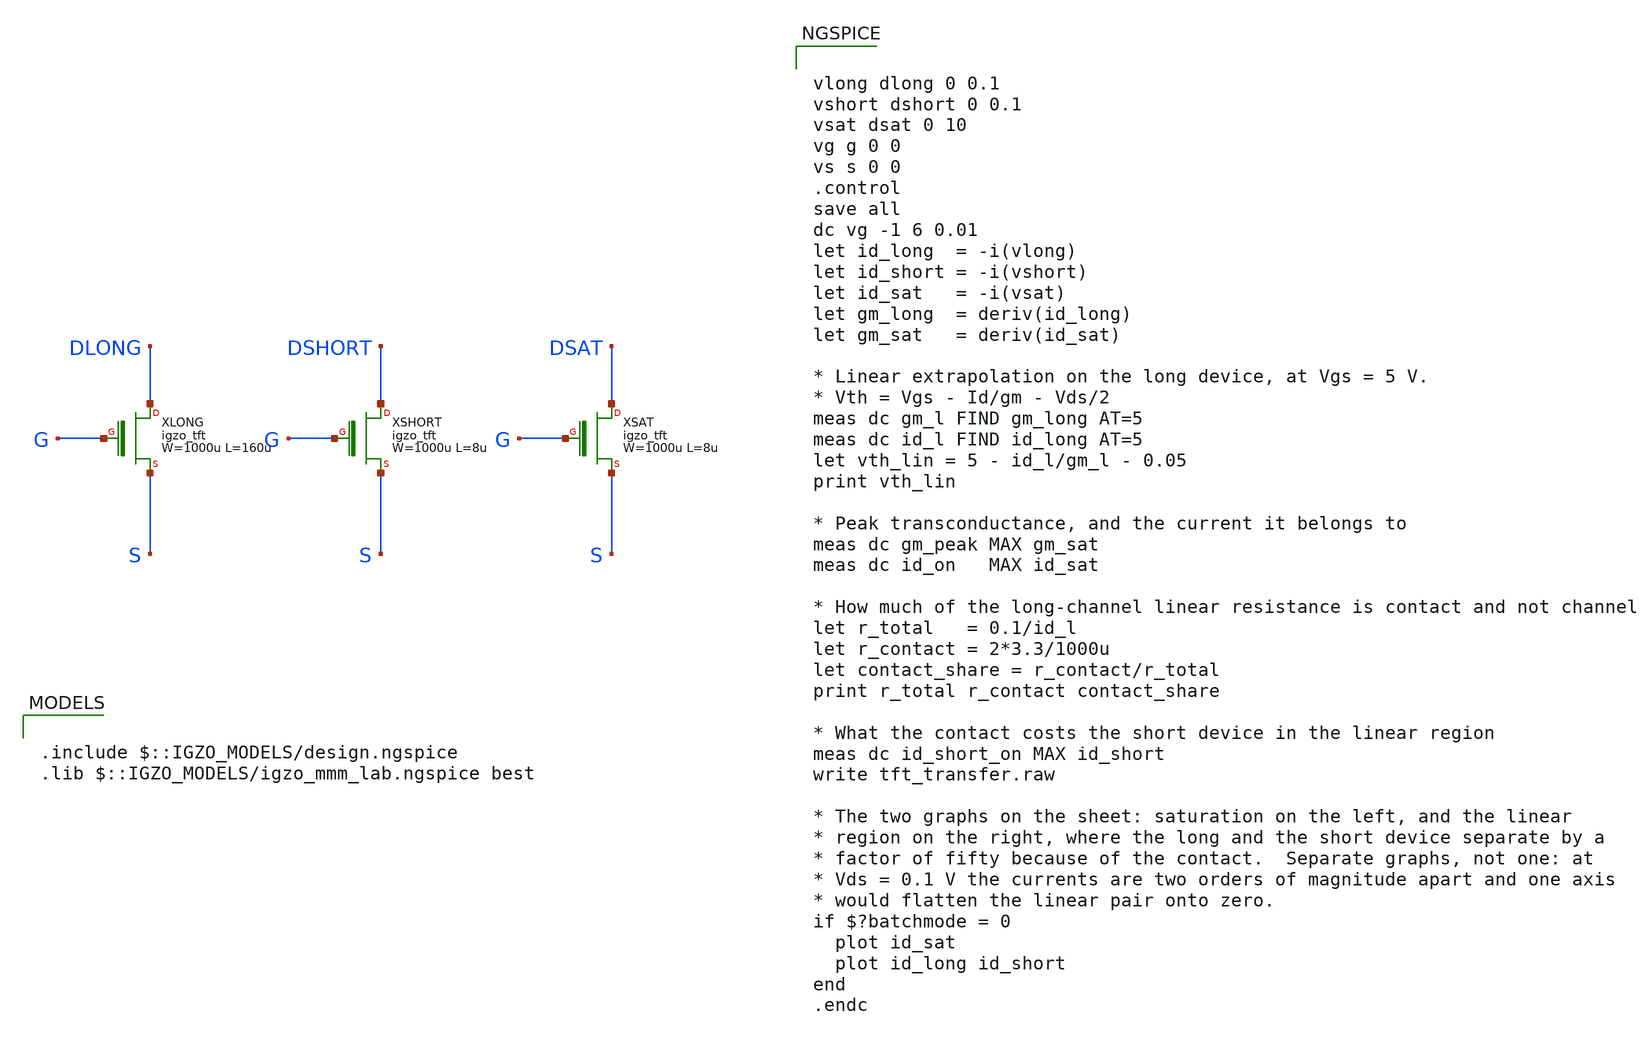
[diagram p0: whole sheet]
** sch_path: libs.tech/xschem/tests/tft_transfer.sch
**.subckt tft_transfer
XXLONG DLONG G S igzo_tft W=1000u L=160u ov=5u nf=1 m=1
XXSHORT DSHORT G S igzo_tft W=1000u L=8u ov=5u nf=1 m=1
XXSAT DSAT G S igzo_tft W=1000u L=8u ov=5u nf=1 m=1
**** begin user architecture code

.include $::IGZO_MODELS/design.ngspice
.lib $::IGZO_MODELS/igzo_mmm_lab.ngspice best



vlong dlong 0 0.1
vshort dshort 0 0.1
vsat dsat 0 10
vg g 0 0
vs s 0 0
.control
save all
dc vg -1 6 0.01
let id_long  = -i(vlong)
let id_short = -i(vshort)
let id_sat   = -i(vsat)
let gm_long  = deriv(id_long)
let gm_sat   = deriv(id_sat)

* Linear extrapolation on the long device, at Vgs = 5 V.
* Vth = Vgs - Id/gm - Vds/2
meas dc gm_l FIND gm_long AT=5
meas dc id_l FIND id_long AT=5
let vth_lin = 5 - id_l/gm_l - 0.05
print vth_lin

* Peak transconductance, and the current it belongs to
meas dc gm_peak MAX gm_sat
meas dc id_on   MAX id_sat

* How much of the long-channel linear resistance is contact and not channel
let r_total   = 0.1/id_l
let r_contact = 2*3.3/1000u
let contact_share = r_contact/r_total
print r_total r_contact contact_share

* What the contact costs the short device in the linear region
meas dc id_short_on MAX id_short
write tft_transfer.raw

* The two graphs on the sheet: saturation on the left, and the linear
* region on the right, where the long and the short device separate by a
* factor of fifty because of the contact.  Separate graphs, not one: at
* Vds = 0.1 V the currents are two orders of magnitude apart and one axis
* would flatten the linear pair onto zero.
if $?batchmode = 0
  plot id_sat
  plot id_long id_short
end
.endc


**** end user architecture code
**.ends
.end
